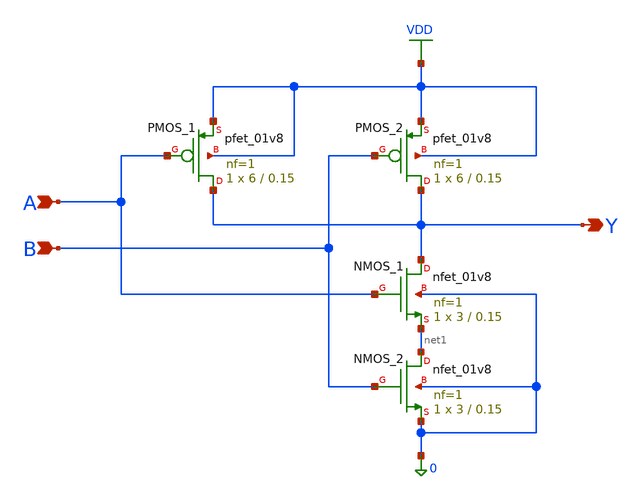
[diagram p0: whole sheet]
** sch_path: cells/full_adder_tg/xschem/nand2_design.sch
**.subckt nand2_design A B Y
*.ipin A
*.ipin B
*.opin Y
XPMOS_1 Y A VDD VDD sky130_fd_pr__pfet_01v8 L=0.15 W=6 nf=1 ad='int((1 + 1)/2) * 6 / 1 * 0.29' as='int((1 + 2)/2) * 6 / 1 * 0.29'
+ pd='2*int((1 + 1)/2) * (6 / 1 + 0.29)' ps='2*int((1 + 2)/2) * (6 / 1 + 0.29)' nrd='0.29 / 6 ' nrs='0.29 / 6 '
+ sa=0 sb=0 sd=0 mult=1 m=1
XPMOS_2 Y B VDD VDD sky130_fd_pr__pfet_01v8 L=0.15 W=6 nf=1 ad='int((1 + 1)/2) * 6 / 1 * 0.29' as='int((1 + 2)/2) * 6 / 1 * 0.29'
+ pd='2*int((1 + 1)/2) * (6 / 1 + 0.29)' ps='2*int((1 + 2)/2) * (6 / 1 + 0.29)' nrd='0.29 / 6 ' nrs='0.29 / 6 '
+ sa=0 sb=0 sd=0 mult=1 m=1
XNMOS_1 Y A net1 0 sky130_fd_pr__nfet_01v8 L=0.15 W=3 nf=1 ad='int((1 + 1)/2) * 3 / 1 * 0.29' as='int((1 + 2)/2) * 3 / 1 * 0.29'
+ pd='2*int((1 + 1)/2) * (3 / 1 + 0.29)' ps='2*int((1 + 2)/2) * (3 / 1 + 0.29)' nrd='0.29 / 3 ' nrs='0.29 / 3 '
+ sa=0 sb=0 sd=0 mult=1 m=1
XNMOS_2 net1 B 0 0 sky130_fd_pr__nfet_01v8 L=0.15 W=3 nf=1 ad='int((1 + 1)/2) * 3 / 1 * 0.29' as='int((1 + 2)/2) * 3 / 1 * 0.29'
+ pd='2*int((1 + 1)/2) * (3 / 1 + 0.29)' ps='2*int((1 + 2)/2) * (3 / 1 + 0.29)' nrd='0.29 / 3 ' nrs='0.29 / 3 '
+ sa=0 sb=0 sd=0 mult=1 m=1
**.ends
.GLOBAL VDD
.end
